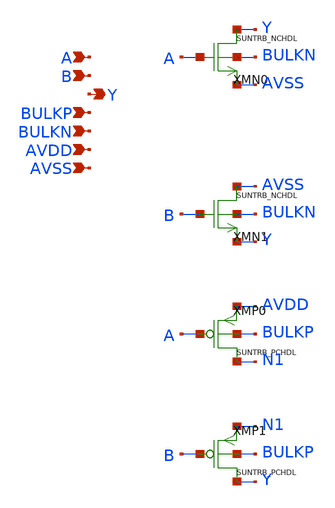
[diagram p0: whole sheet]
** sch_path: design/SUN_TRB_SKY130NM/SUNTRB_NRX1_CV.sch
**.subckt SUNTRB_NRX1_CV A B Y BULKP BULKN AVDD AVSS
*.ipin A
*.ipin B
*.opin Y
*.ipin BULKP
*.ipin BULKN
*.ipin AVDD
*.ipin AVSS
XMN0 Y A AVSS BULKN SUNTRB_NCHDL xoffset=0 yoffset=0 angle=0
XMN1 AVSS B Y BULKN SUNTRB_NCHDL xoffset=0 yoffset=0 angle=0
XMP0 N1 A AVDD BULKP SUNTRB_PCHDL xoffset=0 yoffset=0 angle=0 M=1
XMP1 Y B N1 BULKP SUNTRB_PCHDL xoffset=0 yoffset=0 angle=0 M=1
**.ends
.end
